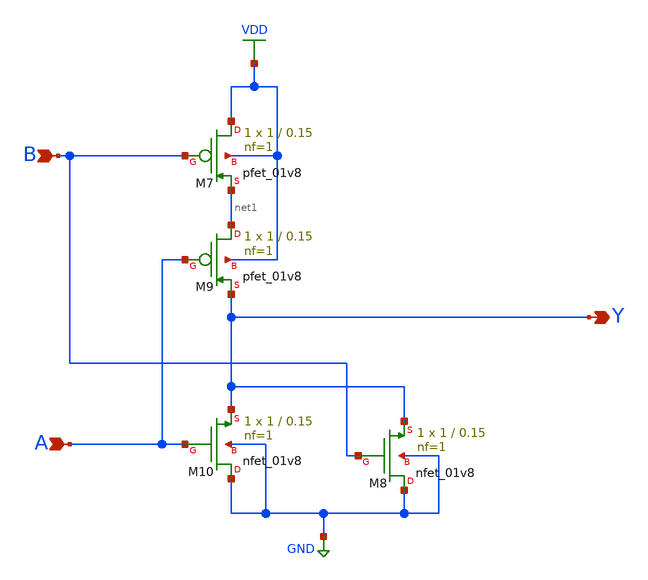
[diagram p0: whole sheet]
** sch_path: gates/NOR2.sch
**.subckt NOR2 A B Y
*.ipin A
*.ipin B
*.opin Y
XM7 VDD B net1 VDD sky130_fd_pr__pfet_01v8 L=0.15 W=1 nf=1 ad='int((nf+1)/2) * W/nf * 0.29' as='int((nf+2)/2) * W/nf * 0.29'
+ pd='2*int((nf+1)/2) * (W/nf + 0.29)' ps='2*int((nf+2)/2) * (W/nf + 0.29)' nrd='0.29 / W' nrs='0.29 / W'
+ sa=0 sb=0 sd=0 mult=1 m=1
XM8 GND B Y GND sky130_fd_pr__nfet_01v8 L=0.15 W=1 nf=1 ad='int((nf+1)/2) * W/nf * 0.29' as='int((nf+2)/2) * W/nf * 0.29'
+ pd='2*int((nf+1)/2) * (W/nf + 0.29)' ps='2*int((nf+2)/2) * (W/nf + 0.29)' nrd='0.29 / W' nrs='0.29 / W'
+ sa=0 sb=0 sd=0 mult=1 m=1
XM9 net1 A Y VDD sky130_fd_pr__pfet_01v8 L=0.15 W=1 nf=1 ad='int((nf+1)/2) * W/nf * 0.29' as='int((nf+2)/2) * W/nf * 0.29'
+ pd='2*int((nf+1)/2) * (W/nf + 0.29)' ps='2*int((nf+2)/2) * (W/nf + 0.29)' nrd='0.29 / W' nrs='0.29 / W'
+ sa=0 sb=0 sd=0 mult=1 m=1
XM10 GND A Y GND sky130_fd_pr__nfet_01v8 L=0.15 W=1 nf=1 ad='int((nf+1)/2) * W/nf * 0.29' as='int((nf+2)/2) * W/nf * 0.29'
+ pd='2*int((nf+1)/2) * (W/nf + 0.29)' ps='2*int((nf+2)/2) * (W/nf + 0.29)' nrd='0.29 / W' nrs='0.29 / W'
+ sa=0 sb=0 sd=0 mult=1 m=1
**.ends
.GLOBAL VDD
.GLOBAL GND
.end
